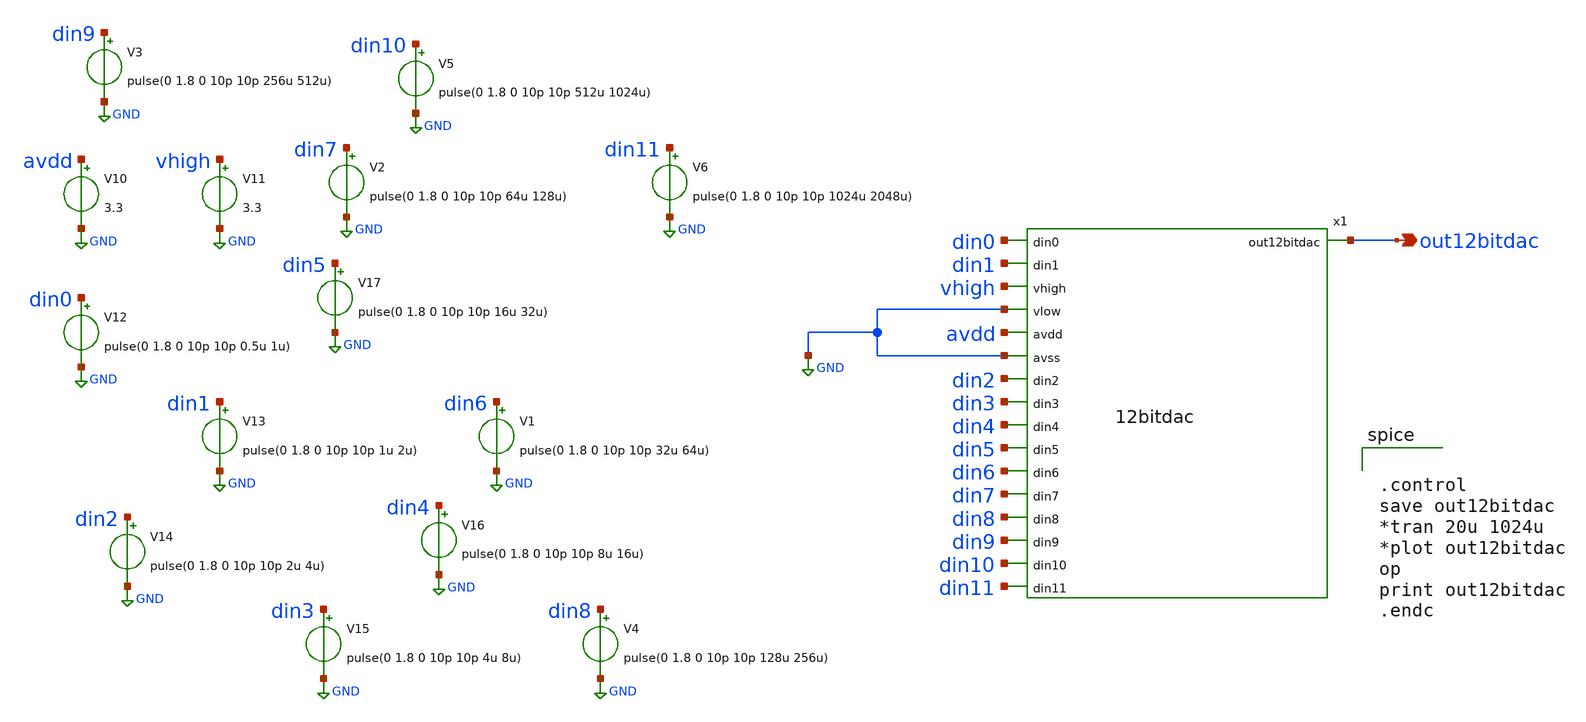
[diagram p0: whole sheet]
** sch_path: xschem/tb_12bitdac.sch
**.subckt tb_12bitdac out12bitdac
*.opin out12bitdac
x1 out12bitdac din0 din1 vhigh GND avdd GND din2 din3 din4 din5 din6 din7 din8 din9 din10 din11
+ 12bitdac
V10 avdd GND 3.3
V11 vhigh GND 3.3
V12 din0 GND pulse(0 1.8 0 10p 10p 0.5u 1u)
V13 din1 GND pulse(0 1.8 0 10p 10p 1u 2u)
V14 din2 GND pulse(0 1.8 0 10p 10p 2u 4u)
V15 din3 GND pulse(0 1.8 0 10p 10p 4u 8u)
V16 din4 GND pulse(0 1.8 0 10p 10p 8u 16u)
V17 din5 GND pulse(0 1.8 0 10p 10p 16u 32u)
V1 din6 GND pulse(0 1.8 0 10p 10p 32u 64u)
V2 din7 GND pulse(0 1.8 0 10p 10p 64u 128u)
V3 din9 GND pulse(0 1.8 0 10p 10p 256u 512u)
V4 din8 GND pulse(0 1.8 0 10p 10p 128u 256u)
V5 din10 GND pulse(0 1.8 0 10p 10p 512u 1024u)
V6 din11 GND pulse(0 1.8 0 10p 10p 1024u 2048u)
**** begin user architecture code


.control
save out12bitdac
*tran 20u 1024u
*plot out12bitdac
op
print out12bitdac
.endc


** opencircuitdesign pdks install
.lib $::SKYWATER_MODELS/sky130.lib.spice tt


**** end user architecture code
**.ends
.GLOBAL GND
.end
